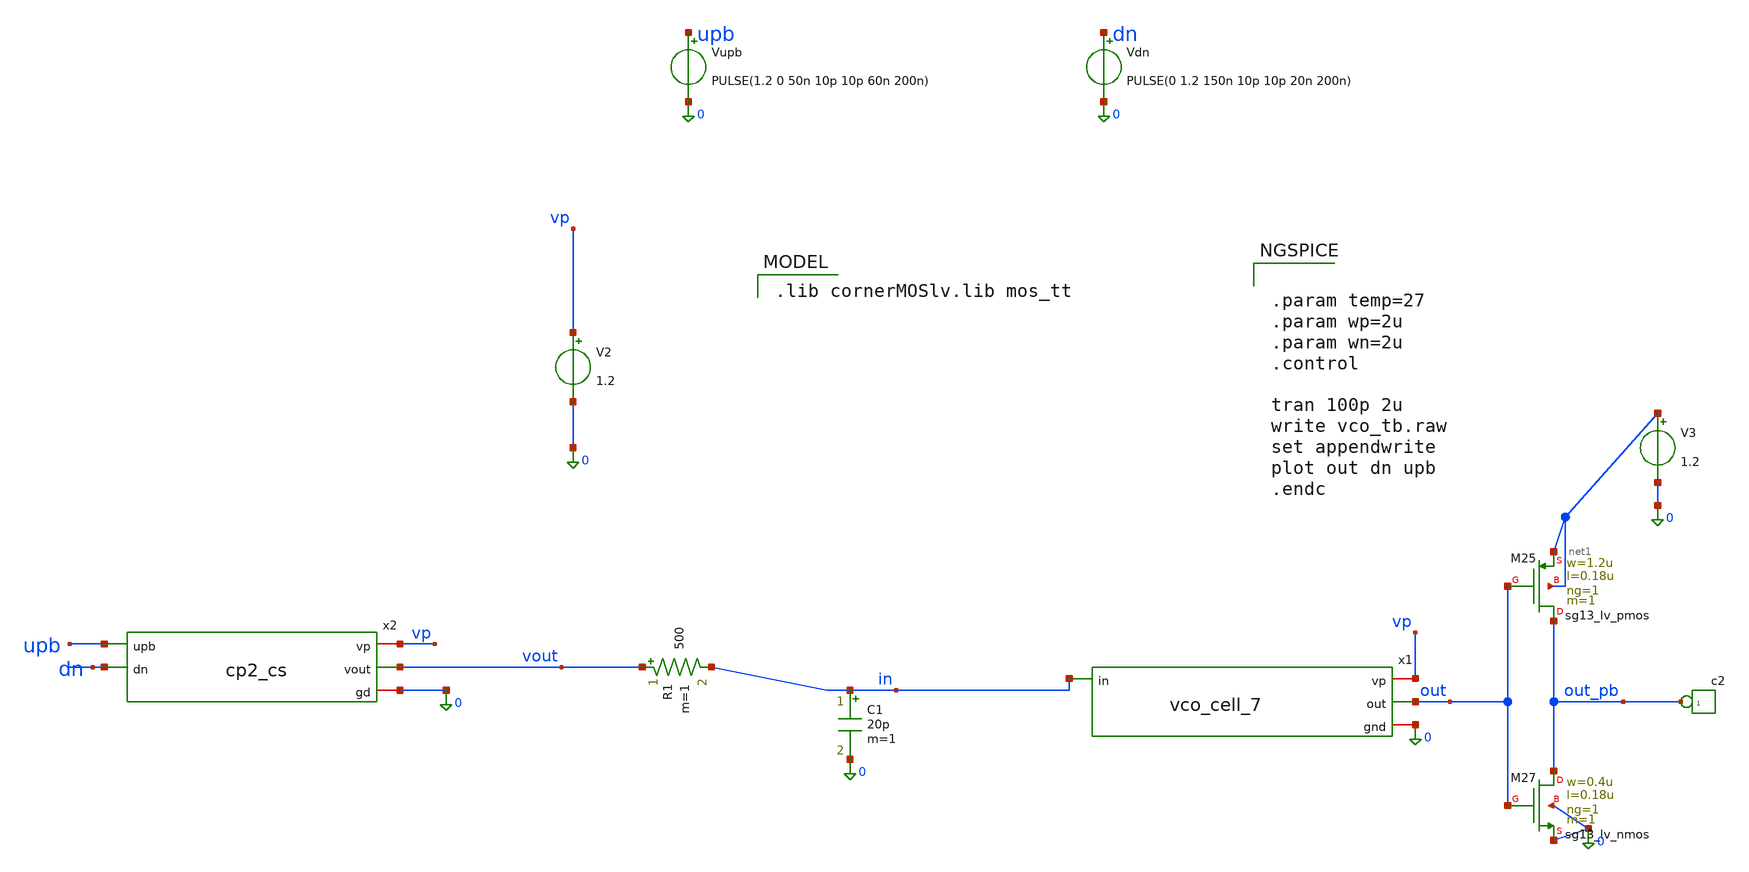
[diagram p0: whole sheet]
** sch_path: PLL0663-main/testbenches/tran/xschem/charge_pump/cp_vco_tb.sch
**.subckt cp_vco_tb
V2 vp 0 1.2
*connector(1,1) ?1 out_pb
XM25 out_pb out net1 net1 sg13_lv_pmos w=1.2u l=0.18u ng=1 m=1 mm_ok=1
XM27 out_pb out 0 0 sg13_lv_nmos w=0.4u l=0.18u ng=1 m=1 mm_ok=1
V3 net1 0 1.2
C1 in 0 20p m=1
x1 vp out in 0 vco_cell_7
x2 vp upb vout dn 0 cp2_cs
R1 vout in 500 m=1
Vupb upb 0 PULSE(1.2 0 50n 10p 10p 60n 200n)
Vdn dn 0 PULSE(0 1.2 150n 10p 10p 20n 200n)
**** begin user architecture code


.param temp=27
.param wp=2u
.param wn=2u
.control

tran 100p 2u
write vco_tb.raw
set appendwrite
plot out dn upb
.endc


 .lib cornerMOSlv.lib mos_tt

**** end user architecture code
**.ends
.end
